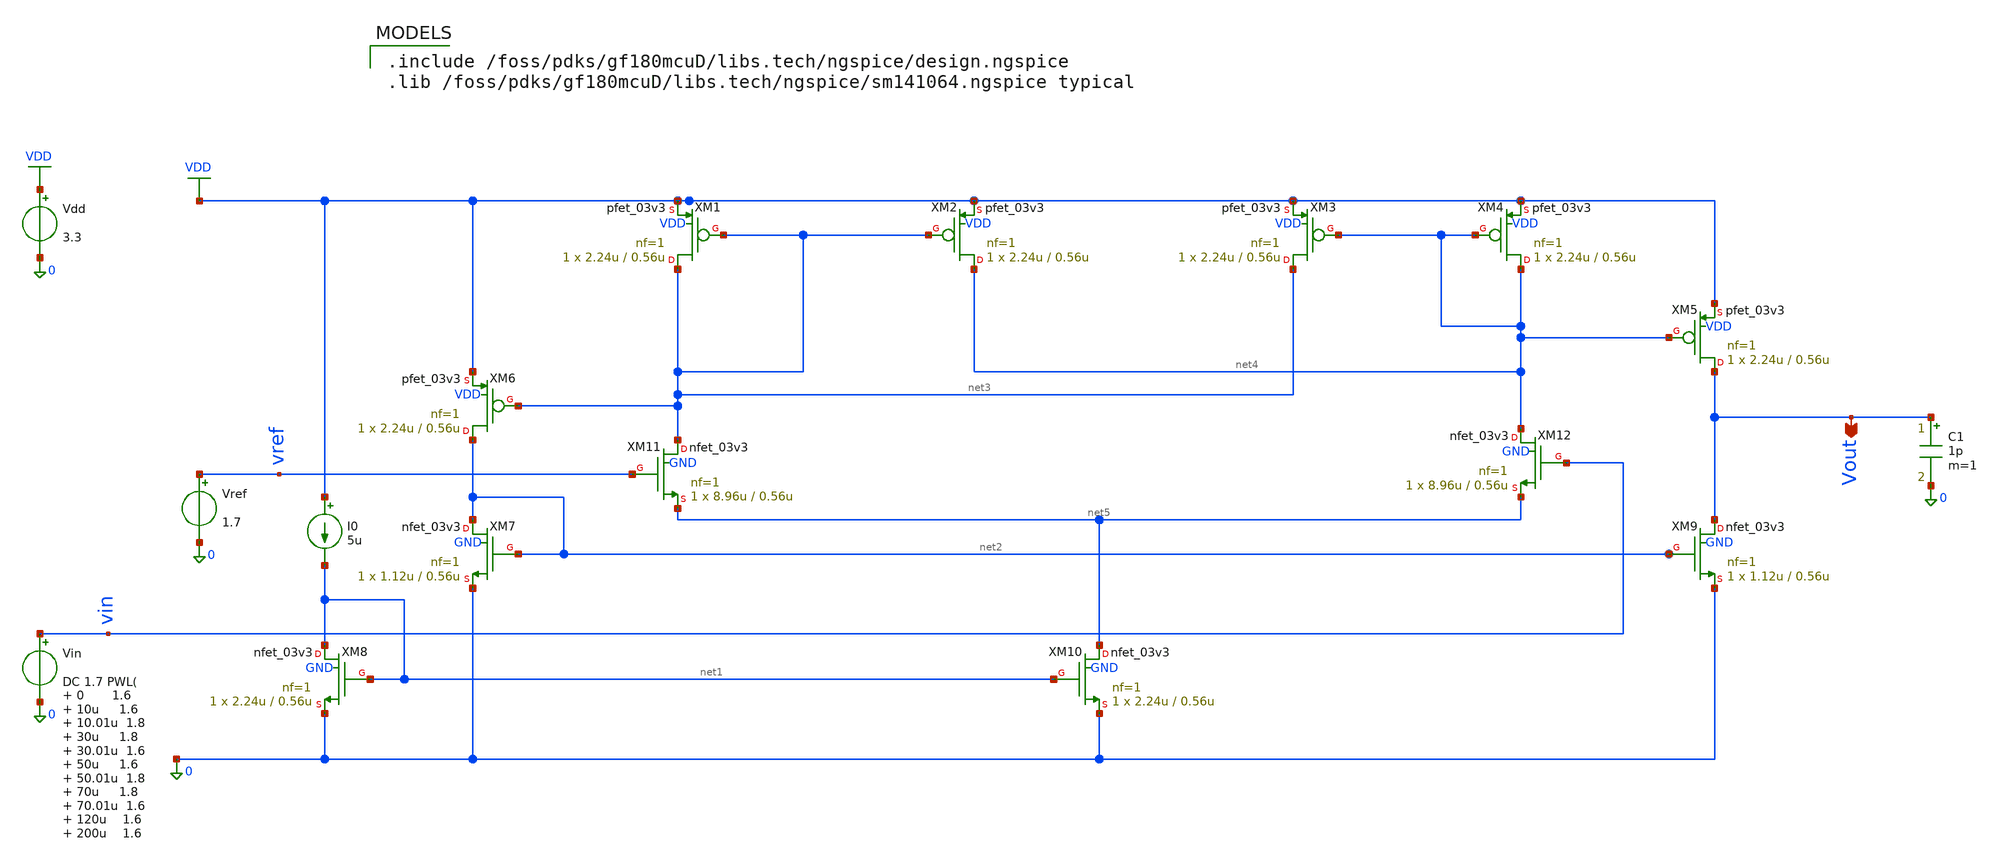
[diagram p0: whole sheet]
** sch_path: comparator/schematic-design/comparator_trans.sch
**.subckt comparator_trans Vout
*.opin Vout
XM1 net3 net3 VDD VDD pfet_03v3 L=0.56u W=2.24u nf=1 ad='int((nf+1)/2) * W/nf * 0.18u' as='int((nf+2)/2) * W/nf * 0.18u'
+ pd='2*int((nf+1)/2) * (W/nf + 0.18u)' ps='2*int((nf+2)/2) * (W/nf + 0.18u)' nrd='0.18u / W' nrs='0.18u / W'
+ sa=0 sb=0 sd=0 m=1 par=1
XM2 net4 net3 VDD VDD pfet_03v3 L=0.56u W=2.24u nf=1 ad='int((nf+1)/2) * W/nf * 0.18u' as='int((nf+2)/2) * W/nf * 0.18u'
+ pd='2*int((nf+1)/2) * (W/nf + 0.18u)' ps='2*int((nf+2)/2) * (W/nf + 0.18u)' nrd='0.18u / W' nrs='0.18u / W'
+ sa=0 sb=0 sd=0 m=1 par=1
XM3 net3 net4 VDD VDD pfet_03v3 L=0.56u W=2.24u nf=1 ad='int((nf+1)/2) * W/nf * 0.18u' as='int((nf+2)/2) * W/nf * 0.18u'
+ pd='2*int((nf+1)/2) * (W/nf + 0.18u)' ps='2*int((nf+2)/2) * (W/nf + 0.18u)' nrd='0.18u / W' nrs='0.18u / W'
+ sa=0 sb=0 sd=0 m=1 par=1
XM4 net4 net4 VDD VDD pfet_03v3 L=0.56u W=2.24u nf=1 ad='int((nf+1)/2) * W/nf * 0.18u' as='int((nf+2)/2) * W/nf * 0.18u'
+ pd='2*int((nf+1)/2) * (W/nf + 0.18u)' ps='2*int((nf+2)/2) * (W/nf + 0.18u)' nrd='0.18u / W' nrs='0.18u / W'
+ sa=0 sb=0 sd=0 m=1 par=1
XM5 Vout net4 VDD VDD pfet_03v3 L=0.56u W=2.24u nf=1 ad='int((nf+1)/2) * W/nf * 0.18u' as='int((nf+2)/2) * W/nf * 0.18u'
+ pd='2*int((nf+1)/2) * (W/nf + 0.18u)' ps='2*int((nf+2)/2) * (W/nf + 0.18u)' nrd='0.18u / W' nrs='0.18u / W'
+ sa=0 sb=0 sd=0 m=1 par=1
XM6 net2 net3 VDD VDD pfet_03v3 L=0.56u W=2.24u nf=1 ad='int((nf+1)/2) * W/nf * 0.18u' as='int((nf+2)/2) * W/nf * 0.18u'
+ pd='2*int((nf+1)/2) * (W/nf + 0.18u)' ps='2*int((nf+2)/2) * (W/nf + 0.18u)' nrd='0.18u / W' nrs='0.18u / W'
+ sa=0 sb=0 sd=0 m=1 par=1
XM7 net2 net2 0 GND nfet_03v3 L=0.56u W=1.12u nf=1 ad='int((nf+1)/2) * W/nf * 0.18u' as='int((nf+2)/2) * W/nf * 0.18u'
+ pd='2*int((nf+1)/2) * (W/nf + 0.18u)' ps='2*int((nf+2)/2) * (W/nf + 0.18u)' nrd='0.18u / W' nrs='0.18u / W'
+ sa=0 sb=0 sd=0 m=1 par=1
XM8 net1 net1 0 GND nfet_03v3 L=0.56u W=2.24u nf=1 ad='int((nf+1)/2) * W/nf * 0.18u' as='int((nf+2)/2) * W/nf * 0.18u'
+ pd='2*int((nf+1)/2) * (W/nf + 0.18u)' ps='2*int((nf+2)/2) * (W/nf + 0.18u)' nrd='0.18u / W' nrs='0.18u / W'
+ sa=0 sb=0 sd=0 m=1 par=1
XM9 Vout net2 0 GND nfet_03v3 L=0.56u W=1.12u nf=1 ad='int((nf+1)/2) * W/nf * 0.18u' as='int((nf+2)/2) * W/nf * 0.18u'
+ pd='2*int((nf+1)/2) * (W/nf + 0.18u)' ps='2*int((nf+2)/2) * (W/nf + 0.18u)' nrd='0.18u / W' nrs='0.18u / W'
+ sa=0 sb=0 sd=0 m=1 par=1
XM10 net5 net1 0 GND nfet_03v3 L=0.56u W=2.24u nf=1 ad='int((nf+1)/2) * W/nf * 0.18u' as='int((nf+2)/2) * W/nf * 0.18u'
+ pd='2*int((nf+1)/2) * (W/nf + 0.18u)' ps='2*int((nf+2)/2) * (W/nf + 0.18u)' nrd='0.18u / W' nrs='0.18u / W'
+ sa=0 sb=0 sd=0 m=1 par=1
XM11 net3 vref net5 GND nfet_03v3 L=0.56u W=8.96u nf=1 ad='int((nf+1)/2) * W/nf * 0.18u' as='int((nf+2)/2) * W/nf * 0.18u'
+ pd='2*int((nf+1)/2) * (W/nf + 0.18u)' ps='2*int((nf+2)/2) * (W/nf + 0.18u)' nrd='0.18u / W' nrs='0.18u / W'
+ sa=0 sb=0 sd=0 m=1 par=1
XM12 net4 vin net5 GND nfet_03v3 L=0.56u W=8.96u nf=1 ad='int((nf+1)/2) * W/nf * 0.18u' as='int((nf+2)/2) * W/nf * 0.18u'
+ pd='2*int((nf+1)/2) * (W/nf + 0.18u)' ps='2*int((nf+2)/2) * (W/nf + 0.18u)' nrd='0.18u / W' nrs='0.18u / W'
+ sa=0 sb=0 sd=0 m=1 par=1
I0 VDD net1 5u
Vref vref 0 1.7
Vin vin 0 DC 1.7 PWL( 0 1.6 10u 1.6 10.01u 1.8 30u 1.8 30.01u 1.6 50u 1.6 50.01u 1.8 70u 1.8 70.01u
+ 1.6 120u 1.6 200u 1.6 300u 1.8 400u 1.6 420u 1.6
)

Vdd VDD 0 3.3
C1 Vout 0 1p m=1
**** begin user architecture code

.include /foss/pdks/gf180mcuD/libs.tech/ngspice/design.ngspice
.lib /foss/pdks/gf180mcuD/libs.tech/ngspice/sm141064.ngspice typical


.control
set noaskquit
save all

*--------------------------------------------------
* 1. DC transfer and nominal offset
*--------------------------------------------------
dc Vin 1.60 1.80 0.1m

meas dc vout_dc_high max v(vout)
meas dc vout_dc_low  min v(vout)
meas dc vtrip_nom find v(vin) when v(vout)=1.65 cross=1

let vos_nom = vtrip_nom - 1.7

print vout_dc_high
print vout_dc_low
print vtrip_nom
print vos_nom

write comparator_dc.raw all

*--------------------------------------------------
* 2. Transient, delay, power and hysteresis
*--------------------------------------------------
tran 10n 420u

write comparator_all_tran.raw all

* Fast switching section: 0 to 120 us
meas tran vin_high  max v(vin)  from=5u to=120u
meas tran vin_low   min v(vin)  from=5u to=120u
meas tran vout_high max v(vout) from=5u to=120u
meas tran vout_low  min v(vout) from=5u to=120u

print vin_high
print vin_low
print vout_high
print vout_low

* Inverting output:
meas tran tpd_rise trig v(vin) val=1.7 rise=1 td=5u targ v(vout) val=1.65 rise=1 td=5u
meas tran tpd_fall trig v(vin) val=1.7 fall=1 td=20u targ v(vout) val=1.65 fall=1 td=20u

print tpd_rise
print tpd_fall

* Average current and power
meas tran idd_avg avg i(Vdd) from=10u to=120u
let pavg = abs(3.3 * idd_avg)

print idd_avg
print pavg

*--------------------------------------------------
* 3. Hysteresis section: 200 to 400 us
* Slow Vin rises from 200 to 300 us,
* then falls from 300 to 400 us.
* For an inverting output:
* rising Vin gives falling Vout,
* falling Vin gives rising Vout.
*--------------------------------------------------
meas tran vtrip_up find v(vin) when v(vout)=1.65 rise=1 td=200u
meas tran vtrip_down find v(vin) when v(vout)=1.65 fall=1 td=300u

let vhyst = abs(vtrip_up - vtrip_down)

print vtrip_up
print vtrip_down
print vhyst

.endc

**** end user architecture code
**.ends
.GLOBAL VDD
.end
